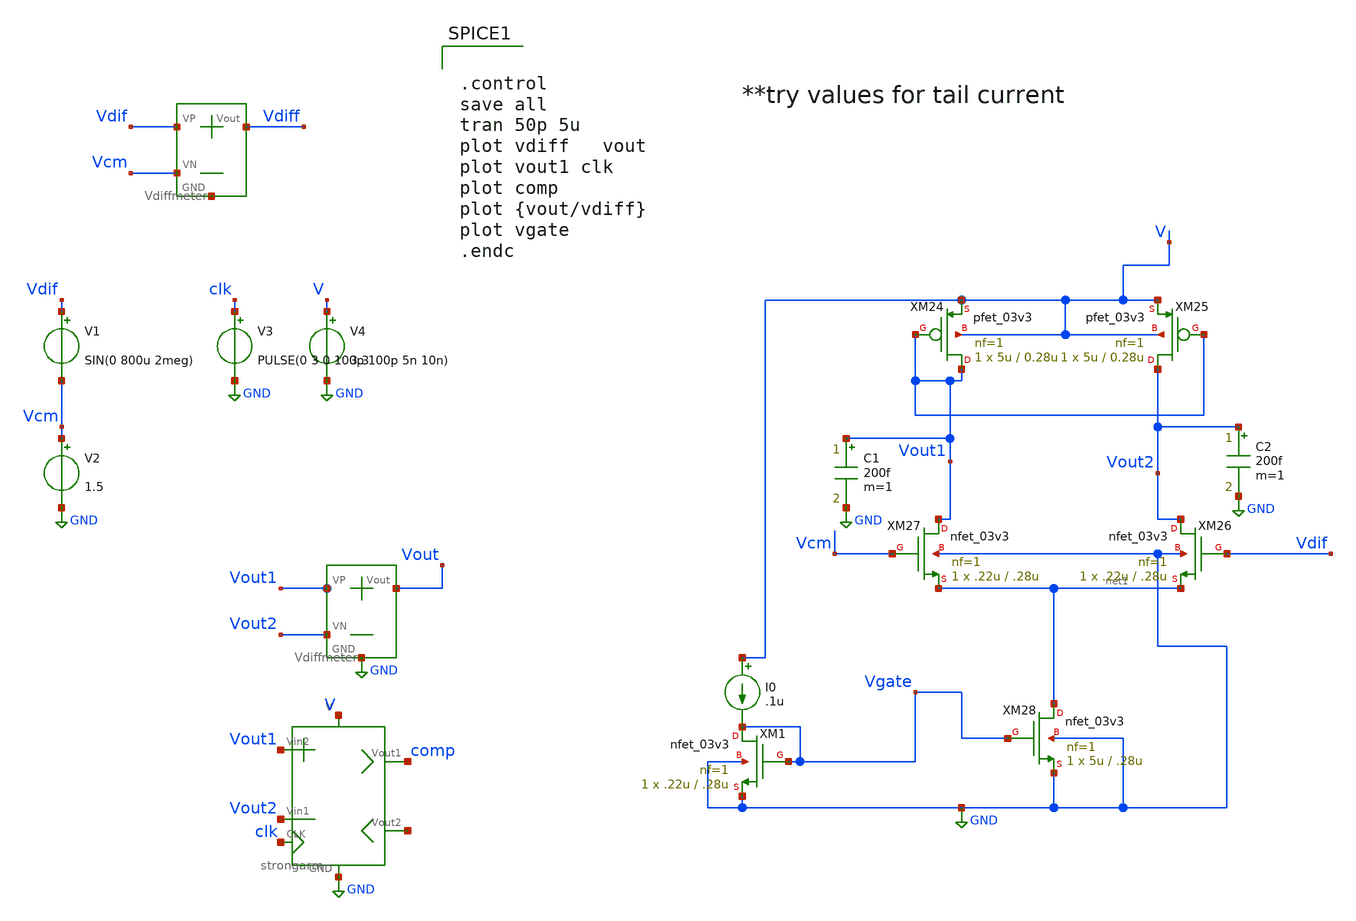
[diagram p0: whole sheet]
** sch_path: SAR_ADC/xschem/test/static_preamp_tb/stat_preamp_sin_8u_tb.sch
**.subckt stat_preamp_sin_8u_tb
V2 Vcm GND 1.5
V3 clk GND PULSE(0 3 0 100p 100p 5n 10n)
V4 V GND 3.3
X4 Vout1 Vout2 Vout GND Vdiffmeter
X1 Vdif Vcm Vdiff net2 Vdiffmeter
X2 V GND Vout2 Vout1 clk comp net3 strongarm
XM26 Vout2 Vdif net1 GND nfet_03v3 L=.28u W=.22u nf=1 ad='int((nf+1)/2) * W/nf * 0.18u' as='int((nf+2)/2) * W/nf * 0.18u'
+ pd='2*int((nf+1)/2) * (W/nf + 0.18u)' ps='2*int((nf+2)/2) * (W/nf + 0.18u)' nrd='0.18u / W' nrs='0.18u / W'
+ sa=0 sb=0 sd=0 m=1
XM27 Vout1 Vcm net1 GND nfet_03v3 L=.28u W=.22u nf=1 ad='int((nf+1)/2) * W/nf * 0.18u' as='int((nf+2)/2) * W/nf * 0.18u'
+ pd='2*int((nf+1)/2) * (W/nf + 0.18u)' ps='2*int((nf+2)/2) * (W/nf + 0.18u)' nrd='0.18u / W' nrs='0.18u / W'
+ sa=0 sb=0 sd=0 m=1
XM28 net1 Vgate GND GND nfet_03v3 L=.28u W=5u nf=1 ad='int((nf+1)/2) * W/nf * 0.18u' as='int((nf+2)/2) * W/nf * 0.18u'
+ pd='2*int((nf+1)/2) * (W/nf + 0.18u)' ps='2*int((nf+2)/2) * (W/nf + 0.18u)' nrd='0.18u / W' nrs='0.18u / W'
+ sa=0 sb=0 sd=0 m=1
XM24 Vout1 Vout1 V V pfet_03v3 L=0.28u W=5u nf=1 ad='int((nf+1)/2) * W/nf * 0.18u' as='int((nf+2)/2) * W/nf * 0.18u'
+ pd='2*int((nf+1)/2) * (W/nf + 0.18u)' ps='2*int((nf+2)/2) * (W/nf + 0.18u)' nrd='0.18u / W' nrs='0.18u / W'
+ sa=0 sb=0 sd=0 m=1
XM25 Vout2 Vout1 V V pfet_03v3 L=0.28u W=5u nf=1 ad='int((nf+1)/2) * W/nf * 0.18u' as='int((nf+2)/2) * W/nf * 0.18u'
+ pd='2*int((nf+1)/2) * (W/nf + 0.18u)' ps='2*int((nf+2)/2) * (W/nf + 0.18u)' nrd='0.18u / W' nrs='0.18u / W'
+ sa=0 sb=0 sd=0 m=1
V1 Vdif Vcm SIN(0 800u 2meg)
I0 V Vgate .1u
XM1 Vgate Vgate GND GND nfet_03v3 L=.28u W=.22u nf=1 ad='int((nf+1)/2) * W/nf * 0.18u' as='int((nf+2)/2) * W/nf * 0.18u'
+ pd='2*int((nf+1)/2) * (W/nf + 0.18u)' ps='2*int((nf+2)/2) * (W/nf + 0.18u)' nrd='0.18u / W' nrs='0.18u / W'
+ sa=0 sb=0 sd=0 m=1
C1 Vout1 GND 200f m=1
C2 Vout2 GND 200f m=1
**** begin user architecture code


.control
save all
tran 50p 5u
plot vdiff   vout
plot vout1 clk
plot comp
plot {vout/vdiff}
plot vgate
.endc


.include /foss/pdks/gf180mcuC/libs.tech/ngspice/design.ngspice
.lib /foss/pdks/gf180mcuC/libs.tech/ngspice/sm141064.ngspice typical

**** end user architecture code
**.ends

* expanding   symbol:  ../../../symbols/Vdiffmeter.sym # of pins=4
** sym_path: SAR_ADC/xschem/spice/symbols/Vdiffmeter.sym
** sch_path: SAR_ADC/xschem/spice/symbols/Vdiffmeter.sch
.subckt Vdiffmeter VP VN Vout GND
*.iopin Vout
*.iopin GND
*.iopin VP
*.iopin VN
R4 Vout GND 1k m=1
E4 Vout GND VP VN 1
.ends


* expanding   symbol:  ../../../symbols/strongarm.sym # of pins=7
** sym_path: SAR_ADC/xschem/designs/strongarm.sym
** sch_path: SAR_ADC/xschem/designs/strongarm.sch
.subckt strongarm V GND Vin1 Vin2 CLK Vout1 Vout2
*.iopin V
*.iopin Vout1
*.iopin Vin1
*.iopin Vin2
*.iopin Vout2
*.iopin CLK
*.iopin GND
XM1 net3 Vout2 V V pfet_03v3 L=0.28u W=2u nf=1 ad='int((nf+1)/2) * W/nf * 0.18u' as='int((nf+2)/2) * W/nf * 0.18u'
+ pd='2*int((nf+1)/2) * (W/nf + 0.18u)' ps='2*int((nf+2)/2) * (W/nf + 0.18u)' nrd='0.18u / W' nrs='0.18u / W'
+ sa=0 sb=0 sd=0 m=1
XM2 Vout1 net1 GND GND nfet_03v3 L=0.28u W=2u nf=1 ad='int((nf+1)/2) * W/nf * 0.18u' as='int((nf+2)/2) * W/nf * 0.18u'
+ pd='2*int((nf+1)/2) * (W/nf + 0.18u)' ps='2*int((nf+2)/2) * (W/nf + 0.18u)' nrd='0.18u / W' nrs='0.18u / W'
+ sa=0 sb=0 sd=0 m=1
XM3 Vout2 Vout1 GND GND nfet_03v3 L=0.28u W=2u nf=1 ad='int((nf+1)/2) * W/nf * 0.18u' as='int((nf+2)/2) * W/nf * 0.18u'
+ pd='2*int((nf+1)/2) * (W/nf + 0.18u)' ps='2*int((nf+2)/2) * (W/nf + 0.18u)' nrd='0.18u / W' nrs='0.18u / W'
+ sa=0 sb=0 sd=0 m=1
XM4 Vout2 net1 GND GND nfet_03v3 L=0.28u W=2u nf=1 ad='int((nf+1)/2) * W/nf * 0.18u' as='int((nf+2)/2) * W/nf * 0.18u'
+ pd='2*int((nf+1)/2) * (W/nf + 0.18u)' ps='2*int((nf+2)/2) * (W/nf + 0.18u)' nrd='0.18u / W' nrs='0.18u / W'
+ sa=0 sb=0 sd=0 m=1
XM5 Vout1 Vout2 GND GND nfet_03v3 L=0.28u W=2u nf=1 ad='int((nf+1)/2) * W/nf * 0.18u' as='int((nf+2)/2) * W/nf * 0.18u'
+ pd='2*int((nf+1)/2) * (W/nf + 0.18u)' ps='2*int((nf+2)/2) * (W/nf + 0.18u)' nrd='0.18u / W' nrs='0.18u / W'
+ sa=0 sb=0 sd=0 m=1
XM6 net2 Vout1 V V pfet_03v3 L=0.28u W=2u nf=1 ad='int((nf+1)/2) * W/nf * 0.18u' as='int((nf+2)/2) * W/nf * 0.18u'
+ pd='2*int((nf+1)/2) * (W/nf + 0.18u)' ps='2*int((nf+2)/2) * (W/nf + 0.18u)' nrd='0.18u / W' nrs='0.18u / W'
+ sa=0 sb=0 sd=0 m=1
XM7 Vout1 Vin1 net3 V pfet_03v3 L=0.28u W=10u nf=1 ad='int((nf+1)/2) * W/nf * 0.18u' as='int((nf+2)/2) * W/nf * 0.18u'
+ pd='2*int((nf+1)/2) * (W/nf + 0.18u)' ps='2*int((nf+2)/2) * (W/nf + 0.18u)' nrd='0.18u / W' nrs='0.18u / W'
+ sa=0 sb=0 sd=0 m=1
XM8 Vout2 Vin2 net2 V pfet_03v3 L=0.28u W=10u nf=1 ad='int((nf+1)/2) * W/nf * 0.18u' as='int((nf+2)/2) * W/nf * 0.18u'
+ pd='2*int((nf+1)/2) * (W/nf + 0.18u)' ps='2*int((nf+2)/2) * (W/nf + 0.18u)' nrd='0.18u / W' nrs='0.18u / W'
+ sa=0 sb=0 sd=0 m=1
x1 V GND net4 CLK inv cl=0.28u wp=0.44u wn=0.22u wx=4u
x2 V GND net1 net4 inv cl=0.28u wp=0.44u wn=0.22u wx=4u
.ends


* expanding   symbol:  inv.sym # of pins=4
** sym_path: SAR_ADC/xschem/designs/inv.sym
** sch_path: SAR_ADC/xschem/designs/inv.sch
.subckt inv vdd gnd vout vin  cl=0.28u wp=0.44u wn=0.22u wx=0.22u
*.ipin gnd
*.ipin vdd
*.ipin vin
*.opin vout
XM1 gnd vin vout gnd nfet_03v3 L=0.28u W=Wx nf=1 ad='int((nf+1)/2) * W/nf * 0.18u' as='int((nf+2)/2) * W/nf * 0.18u'
+ pd='2*int((nf+1)/2) * (W/nf + 0.18u)' ps='2*int((nf+2)/2) * (W/nf + 0.18u)' nrd='0.18u / W' nrs='0.18u / W'
+ sa=0 sb=0 sd=0 m=1
XM2 vdd vin vout vdd pfet_03v3 L=0.28u W=Wx nf=1 ad='int((nf+1)/2) * W/nf * 0.18u' as='int((nf+2)/2) * W/nf * 0.18u'
+ pd='2*int((nf+1)/2) * (W/nf + 0.18u)' ps='2*int((nf+2)/2) * (W/nf + 0.18u)' nrd='0.18u / W' nrs='0.18u / W'
+ sa=0 sb=0 sd=0 m=1
.ends

.GLOBAL GND
.end
